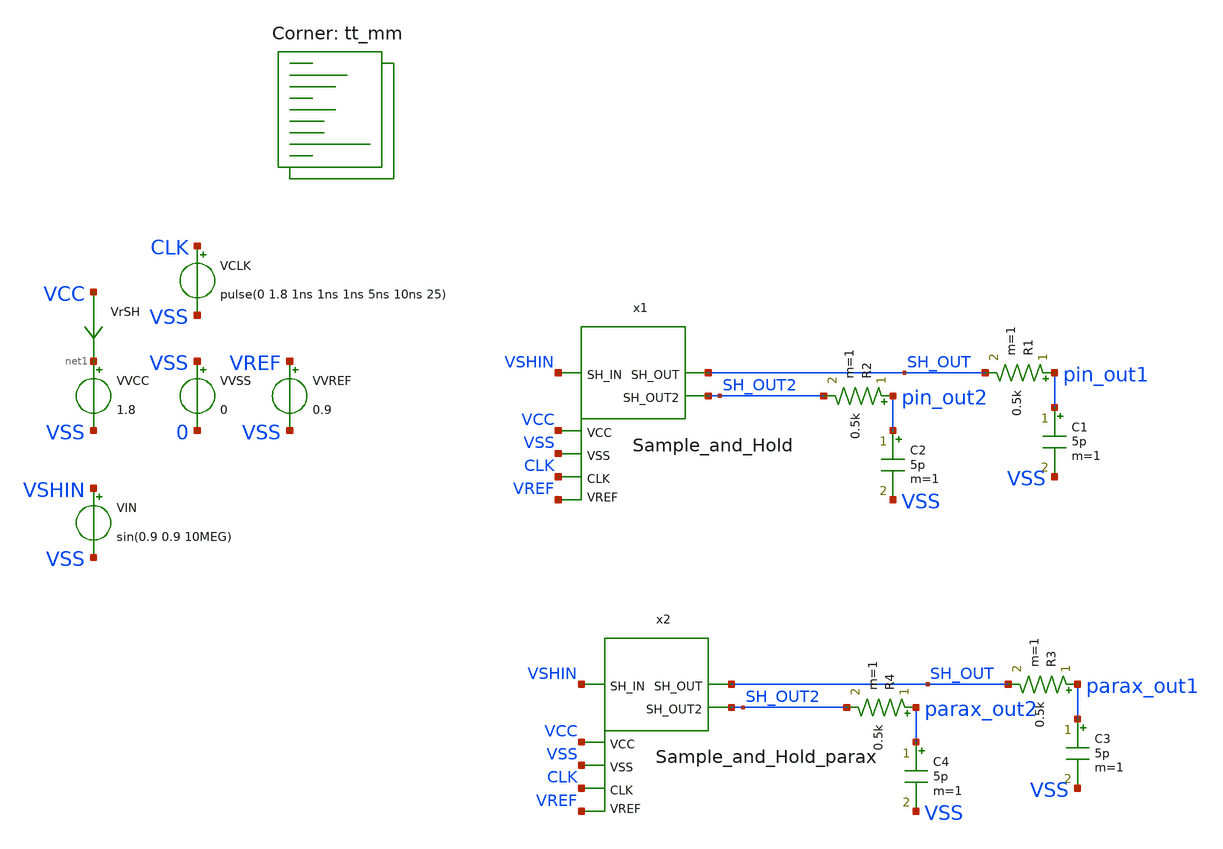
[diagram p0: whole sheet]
** sch_path: xschem/testbench.sch
**.subckt testbench
x1 SH_OUT VSHIN SH_OUT2 VSS VREF VCC CLK Sample_and_Hold
VCLK CLK VSS pulse(0 1.8 1ns 1ns 1ns 5ns 10ns 25)
VVCC net1 VSS 1.8
VVSS VSS 0 0
VIN VSHIN VSS sin(0.9 0.9 10MEG)
VVREF VREF VSS 0.9
R1 pin_out1 SH_OUT 0.5k m=1
R2 pin_out2 SH_OUT2 0.5k m=1
C1 pin_out1 VSS 5p m=1
C2 pin_out2 VSS 5p m=1
VrSH VCC net1 0
.save i(vrsh)
x2 SH_OUT VSHIN SH_OUT2 VSS VREF VCC CLK Sample_and_Hold_parax
R3 parax_out1 SH_OUT 0.5k m=1
R4 parax_out2 SH_OUT2 0.5k m=1
C3 parax_out1 VSS 5p m=1
C4 parax_out2 VSS 5p m=1
**** begin user architecture code
.lib $::SKYWATER_MODELS/sky130.lib.spice tt_mm


.option chgtol=4e-16 method=gear
.param VCC = 1.8
.param VREF = 0.9
.param temp = 25
*vvcc VCC 0 1.8
*vvss VSS 0 0
*vvref VREF 0 0.9
*vclk CLK pulse(1ns 1ns 1ns 5ns 10ns 25)
*vvshin VSHIN sin(0.9 0.9 10MEG)


.control
  save all
  savecurrents
  op
  write testbench.raw
  reset
  set appendwrite
  repeat 5
    save all
    tran 0.1n 250n uic
    write testbench.raw
    set appendwrite
    reset
  end
  quit 0
.endc

**** end user architecture code
**.ends

* expanding   symbol:  Sample_and_Hold.sym # of pins=7
** sym_path: xschem/Sample_and_Hold.sym
** sch_path: xschem/Sample_and_Hold.sch
.subckt Sample_and_Hold SH_OUT SH_IN SH_OUT2 VSS VREF VCC CLK
*.ipin SH_IN
*.ipin CLK
*.opin SH_OUT
*.ipin VSS
*.ipin VCC
*.opin SH_OUT2
*.ipin VREF
XM1 net2 CIN net1 VSS sky130_fd_pr__nfet_01v8 L=0.15 W=1 nf=1 ad='int((nf+1)/2) * W/nf * 0.29' as='int((nf+2)/2) * W/nf * 0.29'
+ pd='2*int((nf+1)/2) * (W/nf + 0.29)' ps='2*int((nf+2)/2) * (W/nf + 0.29)' nrd='0.29 / W' nrs='0.29 / W'
+ sa=0 sb=0 sd=0 mult=1 m=1
XM2 SH_OUT SH_OUT net1 VSS sky130_fd_pr__nfet_01v8 L=0.15 W=1 nf=1 ad='int((nf+1)/2) * W/nf * 0.29' as='int((nf+2)/2) * W/nf * 0.29'
+ pd='2*int((nf+1)/2) * (W/nf + 0.29)' ps='2*int((nf+2)/2) * (W/nf + 0.29)' nrd='0.29 / W' nrs='0.29 / W'
+ sa=0 sb=0 sd=0 mult=1 m=1
XM3 net1 VREF VSS VSS sky130_fd_pr__nfet_01v8 L=0.15 W=8 nf=1 ad='int((nf+1)/2) * W/nf * 0.29' as='int((nf+2)/2) * W/nf * 0.29'
+ pd='2*int((nf+1)/2) * (W/nf + 0.29)' ps='2*int((nf+2)/2) * (W/nf + 0.29)' nrd='0.29 / W' nrs='0.29 / W'
+ sa=0 sb=0 sd=0 mult=1 m=1
XM4 net2 net2 VCC VCC sky130_fd_pr__pfet_01v8 L=0.15 W=4 nf=1 ad='int((nf+1)/2) * W/nf * 0.29' as='int((nf+2)/2) * W/nf * 0.29'
+ pd='2*int((nf+1)/2) * (W/nf + 0.29)' ps='2*int((nf+2)/2) * (W/nf + 0.29)' nrd='0.29 / W' nrs='0.29 / W'
+ sa=0 sb=0 sd=0 mult=1 m=1
XM5 SH_OUT net2 VCC VCC sky130_fd_pr__pfet_01v8 L=0.15 W=4 nf=1 ad='int((nf+1)/2) * W/nf * 0.29' as='int((nf+2)/2) * W/nf * 0.29'
+ pd='2*int((nf+1)/2) * (W/nf + 0.29)' ps='2*int((nf+2)/2) * (W/nf + 0.29)' nrd='0.29 / W' nrs='0.29 / W'
+ sa=0 sb=0 sd=0 mult=1 m=1
XC1 CIN VSS sky130_fd_pr__cap_mim_m3_1 W=2 L=2 MF=5 m=5
XM6 CIN CLKN SH_IN VCC sky130_fd_pr__pfet_01v8 L=0.15 W=2 nf=1 ad='int((nf+1)/2) * W/nf * 0.29' as='int((nf+2)/2) * W/nf * 0.29'
+ pd='2*int((nf+1)/2) * (W/nf + 0.29)' ps='2*int((nf+2)/2) * (W/nf + 0.29)' nrd='0.29 / W' nrs='0.29 / W'
+ sa=0 sb=0 sd=0 mult=1 m=1
XM7 SH_IN CLKB CIN VSS sky130_fd_pr__nfet_01v8 L=0.15 W=1 nf=1 ad='int((nf+1)/2) * W/nf * 0.29' as='int((nf+2)/2) * W/nf * 0.29'
+ pd='2*int((nf+1)/2) * (W/nf + 0.29)' ps='2*int((nf+2)/2) * (W/nf + 0.29)' nrd='0.29 / W' nrs='0.29 / W'
+ sa=0 sb=0 sd=0 mult=1 m=1
XM8 CLKN CLK VSS VSS sky130_fd_pr__nfet_01v8 L=0.15 W=1 nf=1 ad='int((nf+1)/2) * W/nf * 0.29' as='int((nf+2)/2) * W/nf * 0.29'
+ pd='2*int((nf+1)/2) * (W/nf + 0.29)' ps='2*int((nf+2)/2) * (W/nf + 0.29)' nrd='0.29 / W' nrs='0.29 / W'
+ sa=0 sb=0 sd=0 mult=1 m=1
XM9 CLKN CLK VCC VCC sky130_fd_pr__pfet_01v8 L=0.15 W=2 nf=1 ad='int((nf+1)/2) * W/nf * 0.29' as='int((nf+2)/2) * W/nf * 0.29'
+ pd='2*int((nf+1)/2) * (W/nf + 0.29)' ps='2*int((nf+2)/2) * (W/nf + 0.29)' nrd='0.29 / W' nrs='0.29 / W'
+ sa=0 sb=0 sd=0 mult=1 m=1
XM10 CLKB CLKN VSS VSS sky130_fd_pr__nfet_01v8 L=0.15 W=1 nf=1 ad='int((nf+1)/2) * W/nf * 0.29' as='int((nf+2)/2) * W/nf * 0.29'
+ pd='2*int((nf+1)/2) * (W/nf + 0.29)' ps='2*int((nf+2)/2) * (W/nf + 0.29)' nrd='0.29 / W' nrs='0.29 / W'
+ sa=0 sb=0 sd=0 mult=1 m=1
XM11 CLKB CLKN VCC VCC sky130_fd_pr__pfet_01v8 L=0.15 W=2 nf=1 ad='int((nf+1)/2) * W/nf * 0.29' as='int((nf+2)/2) * W/nf * 0.29'
+ pd='2*int((nf+1)/2) * (W/nf + 0.29)' ps='2*int((nf+2)/2) * (W/nf + 0.29)' nrd='0.29 / W' nrs='0.29 / W'
+ sa=0 sb=0 sd=0 mult=1 m=1
XC2 CIN2 VSS sky130_fd_pr__cap_mim_m3_1 W=5 L=5 MF=5 m=5
XM17 CIN2 CLKN SH_IN VCC sky130_fd_pr__pfet_01v8 L=0.15 W=2 nf=1 ad='int((nf+1)/2) * W/nf * 0.29' as='int((nf+2)/2) * W/nf * 0.29'
+ pd='2*int((nf+1)/2) * (W/nf + 0.29)' ps='2*int((nf+2)/2) * (W/nf + 0.29)' nrd='0.29 / W' nrs='0.29 / W'
+ sa=0 sb=0 sd=0 mult=1 m=1
XM18 SH_IN CLKB CIN2 VSS sky130_fd_pr__nfet_01v8 L=0.15 W=1 nf=1 ad='int((nf+1)/2) * W/nf * 0.29' as='int((nf+2)/2) * W/nf * 0.29'
+ pd='2*int((nf+1)/2) * (W/nf + 0.29)' ps='2*int((nf+2)/2) * (W/nf + 0.29)' nrd='0.29 / W' nrs='0.29 / W'
+ sa=0 sb=0 sd=0 mult=1 m=1
XM12 net4 CIN2 net3 VSS sky130_fd_pr__nfet_01v8 L=0.15 W=1 nf=1 ad='int((nf+1)/2) * W/nf * 0.29' as='int((nf+2)/2) * W/nf * 0.29'
+ pd='2*int((nf+1)/2) * (W/nf + 0.29)' ps='2*int((nf+2)/2) * (W/nf + 0.29)' nrd='0.29 / W' nrs='0.29 / W'
+ sa=0 sb=0 sd=0 mult=1 m=1
XM13 SH_OUT2 SH_OUT2 net3 VSS sky130_fd_pr__nfet_01v8 L=0.15 W=1 nf=1 ad='int((nf+1)/2) * W/nf * 0.29'
+ as='int((nf+2)/2) * W/nf * 0.29' pd='2*int((nf+1)/2) * (W/nf + 0.29)' ps='2*int((nf+2)/2) * (W/nf + 0.29)'
+ nrd='0.29 / W' nrs='0.29 / W' sa=0 sb=0 sd=0 mult=1 m=1
XM14 net3 VREF VSS VSS sky130_fd_pr__nfet_01v8 L=0.15 W=8 nf=1 ad='int((nf+1)/2) * W/nf * 0.29' as='int((nf+2)/2) * W/nf * 0.29'
+ pd='2*int((nf+1)/2) * (W/nf + 0.29)' ps='2*int((nf+2)/2) * (W/nf + 0.29)' nrd='0.29 / W' nrs='0.29 / W'
+ sa=0 sb=0 sd=0 mult=1 m=1
XM15 net4 net4 VCC VCC sky130_fd_pr__pfet_01v8 L=0.15 W=4 nf=1 ad='int((nf+1)/2) * W/nf * 0.29' as='int((nf+2)/2) * W/nf * 0.29'
+ pd='2*int((nf+1)/2) * (W/nf + 0.29)' ps='2*int((nf+2)/2) * (W/nf + 0.29)' nrd='0.29 / W' nrs='0.29 / W'
+ sa=0 sb=0 sd=0 mult=1 m=1
XM16 SH_OUT2 net4 VCC VCC sky130_fd_pr__pfet_01v8 L=0.15 W=4 nf=1 ad='int((nf+1)/2) * W/nf * 0.29' as='int((nf+2)/2) * W/nf * 0.29'
+ pd='2*int((nf+1)/2) * (W/nf + 0.29)' ps='2*int((nf+2)/2) * (W/nf + 0.29)' nrd='0.29 / W' nrs='0.29 / W'
+ sa=0 sb=0 sd=0 mult=1 m=1
.ends


* expanding   symbol:  Sample_and_Hold_parax.sym # of pins=7
** sym_path: xschem/Sample_and_Hold.sym
.include [file normalize ../mag/Sample_and_Hold.sim.spice]
.end
